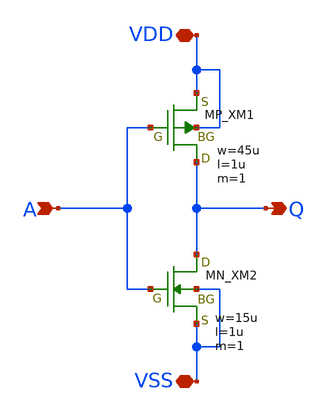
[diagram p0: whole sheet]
** sch_path: schematic/20250924_OSS_Workshop/Qdai/inverter_solo/inv_kayano.sch
**.subckt inv_kayano VDD VSS A Q
*.iopin VDD
*.iopin VSS
*.ipin A
*.opin Q
XM1 Q A VDD VDD PMOS w=45u l=1u as=0 ad=0 ps=0 pd=0 nrd=0 nrs=0 m=1
XM2 Q A VSS VSS NMOS w=15u l=1u as=0 ad=0 ps=0 pd=0 nrd=0 nrs=0 m=1
**.ends
.end
